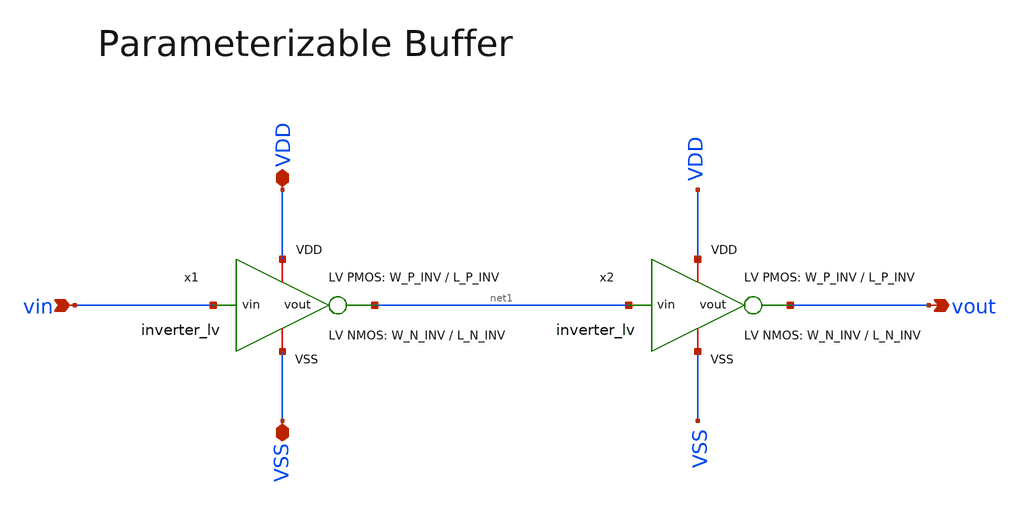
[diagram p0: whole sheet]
** sch_path: SG13G2_ATBS-ADC-main/xschem/buffer/buffer_lv.sch
**.subckt buffer_lv vin VDD VSS vout
*.ipin vin
*.iopin VDD
*.iopin VSS
*.opin vout
x1 VDD vin net1 VSS inverter_lv W_P=W_P_INV L_P=L_P_INV W_N=W_N_INV L_N=L_N_INV
x2 VDD net1 vout VSS inverter_lv W_P=W_P_INV L_P=L_P_INV W_N=W_N_INV L_N=L_N_INV
**.ends

* expanding   symbol:  inverter/inverter_lv.sym # of pins=4
** sym_path: SG13G2_ATBS-ADC-main/xschem/inverter/inverter_lv.sym
** sch_path: SG13G2_ATBS-ADC-main/xschem/inverter/inverter_lv.sch
.subckt inverter_lv VDD vin vout VSS  W_P=3.0u L_P=0.13u W_N=1.0u L_N=0.13u
*.ipin vin
*.iopin VDD
*.iopin VSS
*.opin vout
XM1 vout vin VDD VDD sg13_lv_pmos w=W_P l=L_P ng=1 m=1 mm_ok=1
XM2 vout vin VSS VSS sg13_lv_nmos w=W_N l=L_N ng=1 m=1 mm_ok=1
.ends

.end
